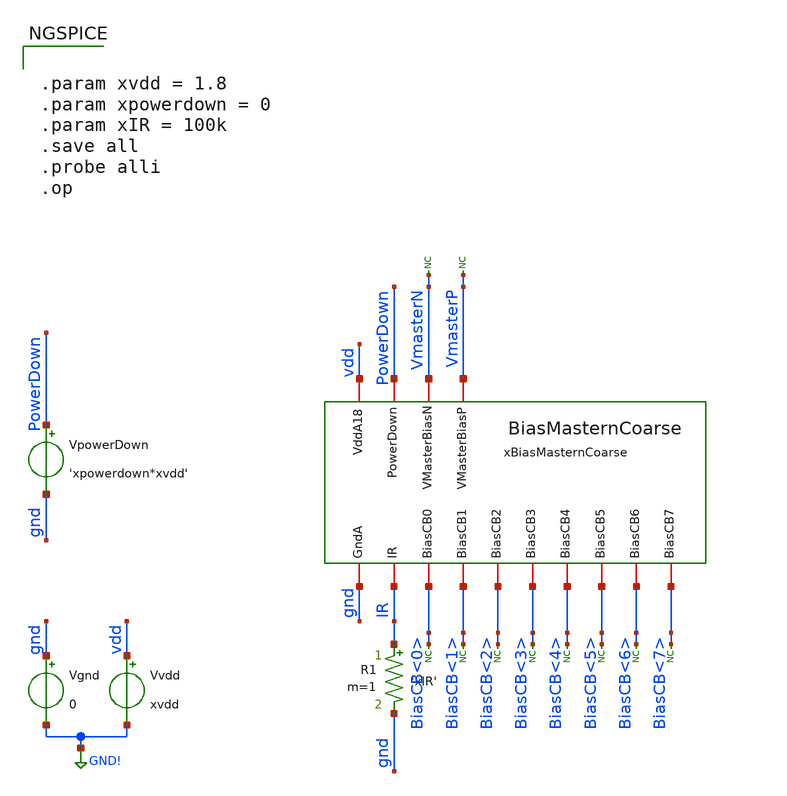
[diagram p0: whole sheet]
** sch_path: analog/klayout/production/final_merge_20260923/testbenches/cace/analog/xschem/tb_BiasMasternCoarse.sch
**.subckt tb_BiasMasternCoarse
xBiasMasternCoarse vdd gnd BiasCB<0> BiasCB<1> BiasCB<3> BiasCB<4> BiasCB<5> BiasCB<6> BiasCB<7>
+ BiasCB<2> PowerDown VmasterN VmasterP IR BiasMasternCoarse
Vgnd gnd GND! 0
.save i(vgnd)
Vvdd vdd GND! xvdd
.save i(vvdd)
R1 IR gnd 'xIR' m=1
VpowerDown PowerDown gnd 'xpowerdown*xvdd'
.save i(vpowerdown)
* noconn VmasterN
* noconn VmasterP
* noconn BiasCB<7>
* noconn BiasCB<6>
* noconn BiasCB<5>
* noconn BiasCB<4>
* noconn BiasCB<3>
* noconn BiasCB<2>
* noconn BiasCB<1>
* noconn BiasCB<0>
**** begin user architecture code

** opencircuitdesign pdks install
.lib $::SKYWATER_MODELS/sky130.lib.spice tt



.param xvdd = 1.8
.param xpowerdown = 0
.param xIR = 100k
.save all
.probe alli
.op


**** end user architecture code
**.ends
.GLOBAL GND!
.end
